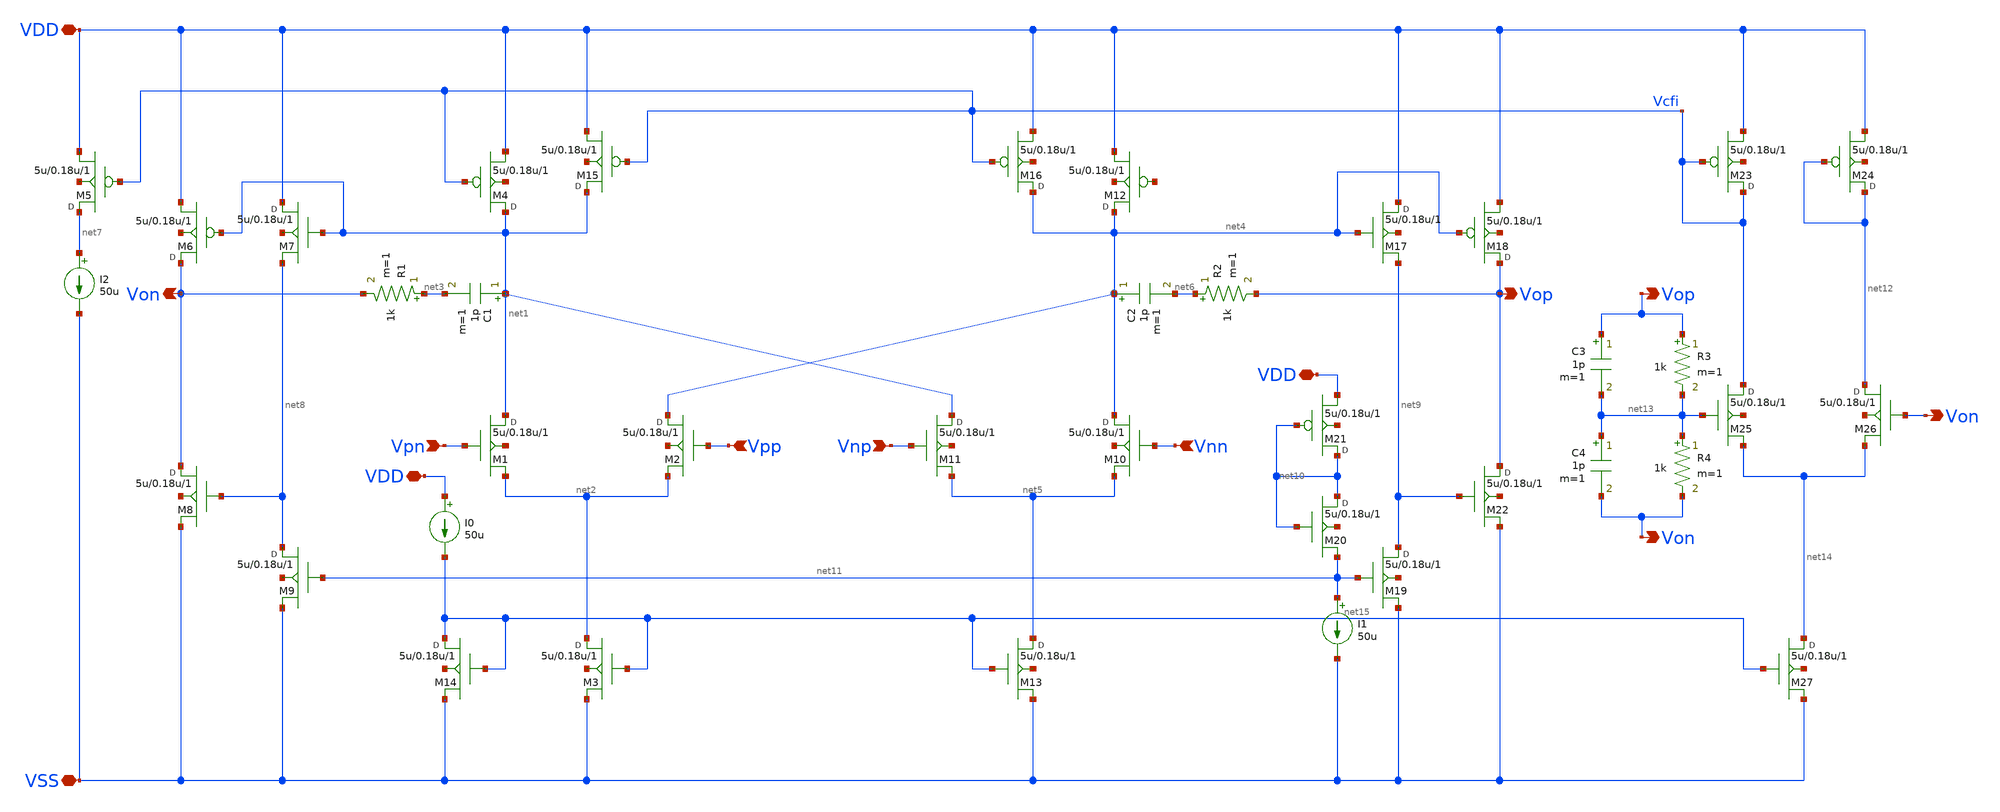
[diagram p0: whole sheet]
** sch_path: fdda.sch
**.subckt fdda Vpn Vpp Vnp Vnn VDD VSS VDD VDD Von Von Vop Vop Von
*.ipin Vpn
*.ipin Vpp
*.ipin Vnp
*.ipin Vnn
*.iopin VDD
*.iopin VSS
*.iopin VDD
*.iopin VDD
*.opin Von
*.opin Von
*.opin Vop
*.opin Vop
*.opin Von
M1 net1 Vpn net2 net16 nmos w=5u l=0.18u m=1
M2 net4 Vpp net2 net17 nmos w=5u l=0.18u m=1
R1 net3 Von 1k m=1
C1 net1 net3 1p m=1
M4 net1 Vcfi VDD net18 pmos w=5u l=0.18u m=1
M3 net2 net15 VSS net19 nmos w=5u l=0.18u m=1
M10 net4 Vnn net5 net20 nmos w=5u l=0.18u m=1
M11 net1 Vnp net5 net21 nmos w=5u l=0.18u m=1
R2 net6 Vop 1k m=1
C2 net4 net6 1p m=1
M12 net4 net22 VDD net23 pmos w=5u l=0.18u m=1
M13 net5 net15 VSS net24 nmos w=5u l=0.18u m=1
M14 net15 net15 VSS net25 nmos w=5u l=0.18u m=1
I0 VDD net15 50u
I1 net11 VSS 50u
I2 net7 VSS 50u
M5 net7 Vcfi VDD net26 pmos w=5u l=0.18u m=1
M6 Von net1 VDD net27 pmos w=5u l=0.18u m=1
M7 VDD net1 net8 net28 nmos w=5u l=0.18u m=1
M8 Von net8 VSS net29 nmos w=5u l=0.18u m=1
M9 net8 net11 VSS net30 nmos w=5u l=0.18u m=1
M15 net1 Vcfi VDD net31 pmos w=5u l=0.18u m=1
M16 net4 Vcfi VDD net32 pmos w=5u l=0.18u m=1
M17 VDD net4 net9 net33 nmos w=5u l=0.18u m=1
M18 Vop net4 VDD net34 pmos w=5u l=0.18u m=1
M19 net9 net11 VSS net35 nmos w=5u l=0.18u m=1
M20 net10 net10 net11 net36 nmos w=5u l=0.18u m=1
M21 net10 net10 VDD net37 pmos w=5u l=0.18u m=1
M22 Vop net9 VSS net38 nmos w=5u l=0.18u m=1
M23 Vcfi Vcfi VDD net39 pmos w=5u l=0.18u m=1
M24 net12 net12 VDD net40 pmos w=5u l=0.18u m=1
M25 Vcfi net13 net14 net41 nmos w=5u l=0.18u m=1
M26 net12 Von net14 net42 nmos w=5u l=0.18u m=1
R3 Vop net13 1k m=1
R4 net13 Von 1k m=1
C3 Vop net13 1p m=1
C4 net13 Von 1p m=1
M27 net14 net15 VSS net43 nmos w=5u l=0.18u m=1
**.ends
.end
